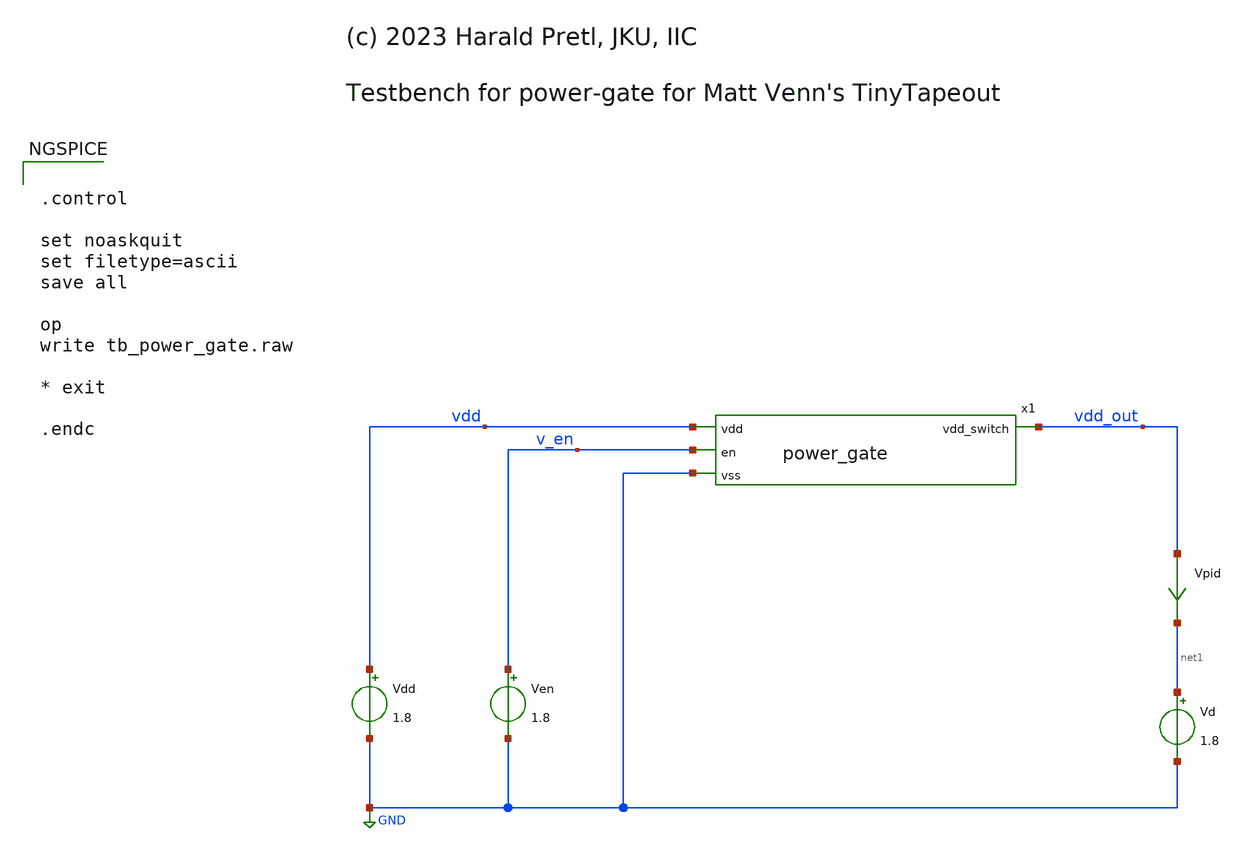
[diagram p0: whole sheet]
** sch_path: tb_power_gate.sch
* (c) 2023 Harald Pretl, JKU, IIC
**.subckt tb_power_gate
Ven v_en GND 1.8
Vdd vdd GND 1.8
Vpid vdd_out net1 0
.save i(vpid)
Vd net1 GND 1.8
x1 vdd v_en vdd_out GND power_gate
**** begin user architecture code
 ** manual skywater pdks install (with patches applied)
* .lib $::SKYWATER_MODELS/models/sky130.lib.spice tt

** opencircuitdesign pdks install
.lib $::SKYWATER_MODELS/sky130.lib.spice.tt.red tt

.param mc_mm_switch=0
.param mc_pr_switch=0



.control

set noaskquit
set filetype=ascii
save all

op
write tb_power_gate.raw

* exit

.endc


**** end user architecture code
**.ends

* expanding   symbol:  /foss/designs/power_gate/power_gate.sym # of pins=4
** sym_path: power_gate.sym
** sch_path: power_gate.sch
.subckt power_gate vdd en vdd_switch vss
*.ipin en
*.opin vdd_switch
*.ipin vdd
*.ipin vss
XM0 vdd_switch en_b vdd vdd sky130_fd_pr__pfet_01v8 L=0.15 W=960 nf=120 ad='int((nf+1)/2) * W/nf * 0.29'
+ as='int((nf+2)/2) * W/nf * 0.29' pd='2*int((nf+1)/2) * (W/nf + 0.29)' ps='2*int((nf+2)/2) * (W/nf + 0.29)'
+ nrd='0.29 / W' nrs='0.29 / W' sa=0 sb=0 sd=0 mult=1 m=1
XM1 en_b en vdd vdd sky130_fd_pr__pfet_01v8 L=0.15 W=8 nf=1 ad='int((nf+1)/2) * W/nf * 0.29' as='int((nf+2)/2) * W/nf * 0.29'
+ pd='2*int((nf+1)/2) * (W/nf + 0.29)' ps='2*int((nf+2)/2) * (W/nf + 0.29)' nrd='0.29 / W' nrs='0.29 / W'
+ sa=0 sb=0 sd=0 mult=1 m=1
XM2 en_b en vss vss sky130_fd_pr__nfet_01v8 L=0.15 W=8 nf=1 ad='int((nf+1)/2) * W/nf * 0.29' as='int((nf+2)/2) * W/nf * 0.29'
+ pd='2*int((nf+1)/2) * (W/nf + 0.29)' ps='2*int((nf+2)/2) * (W/nf + 0.29)' nrd='0.29 / W' nrs='0.29 / W'
+ sa=0 sb=0 sd=0 mult=1 m=1
.ends

.GLOBAL GND
.end
